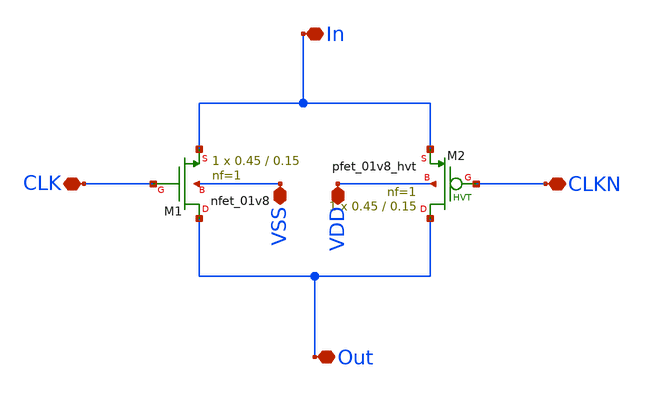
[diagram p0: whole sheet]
** sch_path: HVT/passGate_hvt/passGate_hvt.sch
**.subckt passGate_hvt In CLKN Out VSS VDD CLK
*.iopin In
*.iopin CLKN
*.iopin Out
*.iopin VSS
*.iopin VDD
*.iopin CLK
XM2 Out CLKN In VDD sky130_fd_pr__pfet_01v8_hvt L=0.15 W=0.45 nf=1 ad='int((nf+1)/2) * W/nf * 0.29' as='int((nf+2)/2) * W/nf * 0.29'
+ pd='2*int((nf+1)/2) * (W/nf + 0.29)' ps='2*int((nf+2)/2) * (W/nf + 0.29)' nrd='0.29 / W' nrs='0.29 / W'
+ sa=0 sb=0 sd=0 mult=1 m=1
XM1 Out CLK In VSS sky130_fd_pr__nfet_01v8 L=0.15 W=0.45 nf=1 ad='int((nf+1)/2) * W/nf * 0.29' as='int((nf+2)/2) * W/nf * 0.29'
+ pd='2*int((nf+1)/2) * (W/nf + 0.29)' ps='2*int((nf+2)/2) * (W/nf + 0.29)' nrd='0.29 / W' nrs='0.29 / W'
+ sa=0 sb=0 sd=0 mult=1 m=1
**.ends
.end
